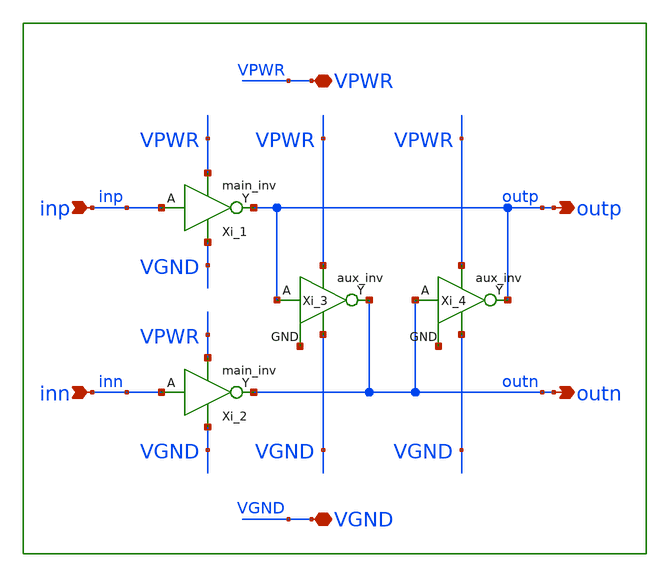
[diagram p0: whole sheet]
** sch_path: xschem/lib/cc_inv.sch
**.subckt cc_inv outp inn VGND outn inp VPWR
*.opin outp
*.ipin inn
*.iopin VGND
*.opin outn
*.ipin inp
*.iopin VPWR
Xi_1 inp VPWR VGND outp main_inv l=l12 wp=wp12 wn=wn12
Xi_3 VPWR VGND outn net1 outp aux_inv
Xi_2 inn VPWR VGND outn main_inv l=l12 wp=wp12 wn=wn12
Xi_4 VPWR VGND outp net2 outn aux_inv
**.ends
.end
